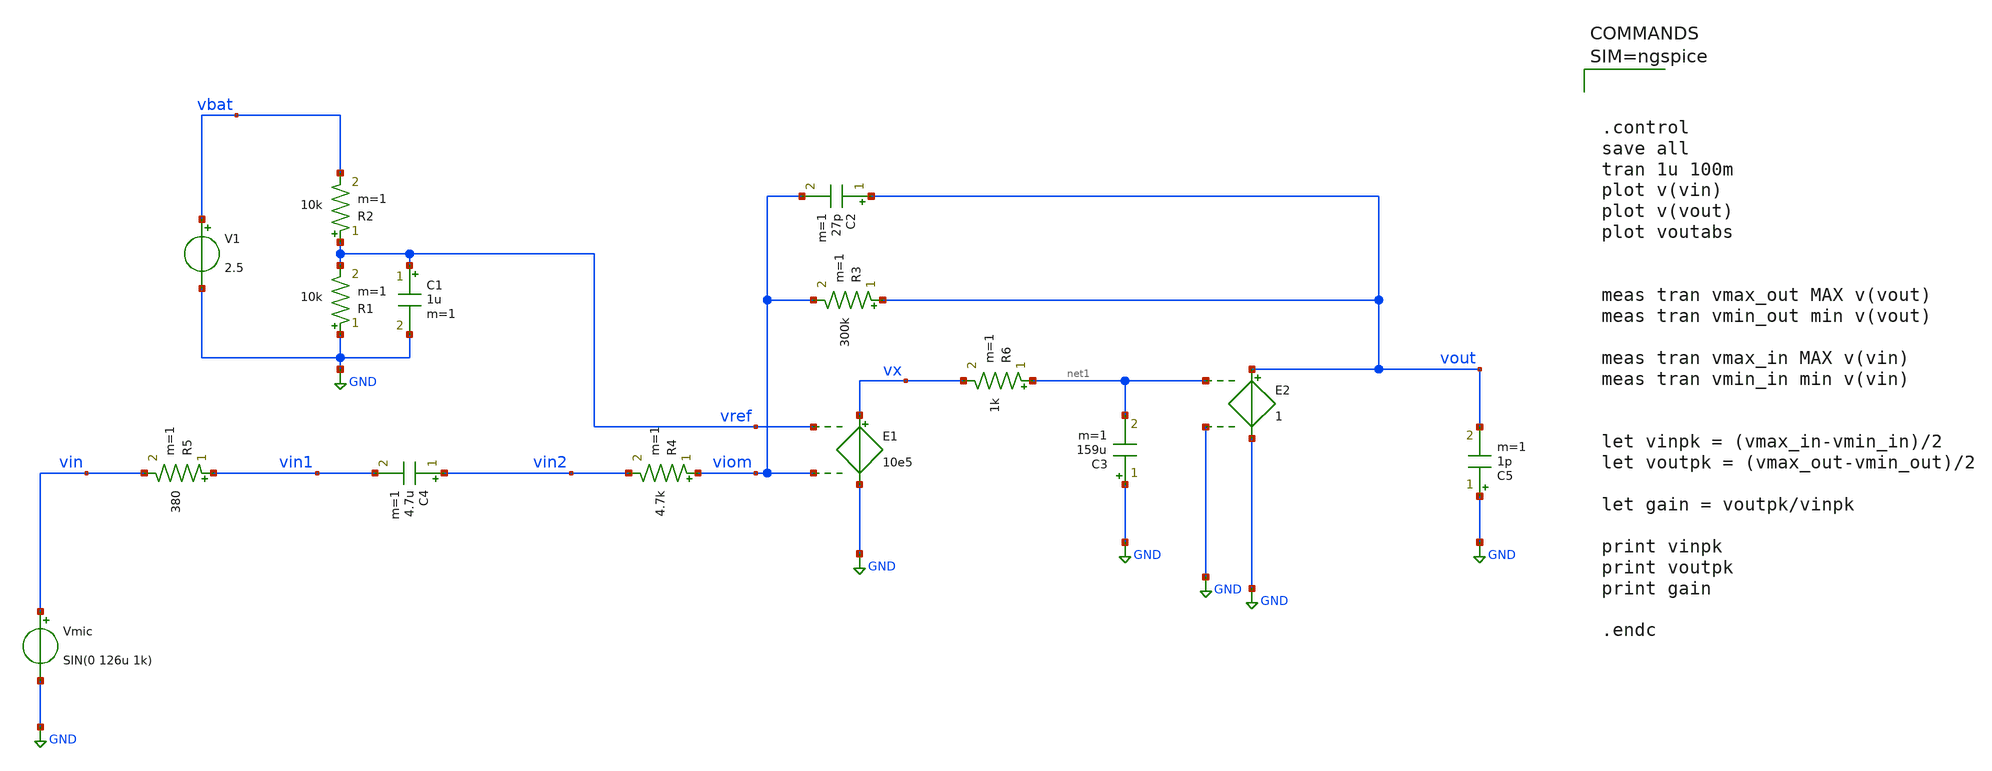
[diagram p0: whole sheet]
** sch_path: xschem/mic_change6.sch
**.subckt mic_change6
R1 GND vref 10k m=1
R2 vref vbat 10k m=1
C1 vref GND 1u m=1
V1 vbat GND 2.5
R3 vout viom 300k m=1
R4 viom vin2 4.7k m=1
R5 vin1 vin 380 m=1
C2 vout viom 27p m=1
E1 vx GND vref viom 10e5
C3 GND net1 159u m=1
C4 vin2 vin1 4.7u m=1
Vmic vin GND SIN(0 126u 1k)
E2 vout GND net1 GND 1
C5 GND vout 1p m=1
R6 net1 vx 1k m=1
**** begin user architecture code




.control
save all
tran 1u 100m
plot v(vin)
plot v(vout)
plot voutabs


meas tran vmax_out MAX v(vout)
meas tran vmin_out min v(vout)

meas tran vmax_in MAX v(vin)
meas tran vmin_in min v(vin)


let vinpk = (vmax_in-vmin_in)/2
let voutpk = (vmax_out-vmin_out)/2

let gain = voutpk/vinpk

print vinpk
print voutpk
print gain

.endc




**** end user architecture code
**.ends
.GLOBAL GND
.end
